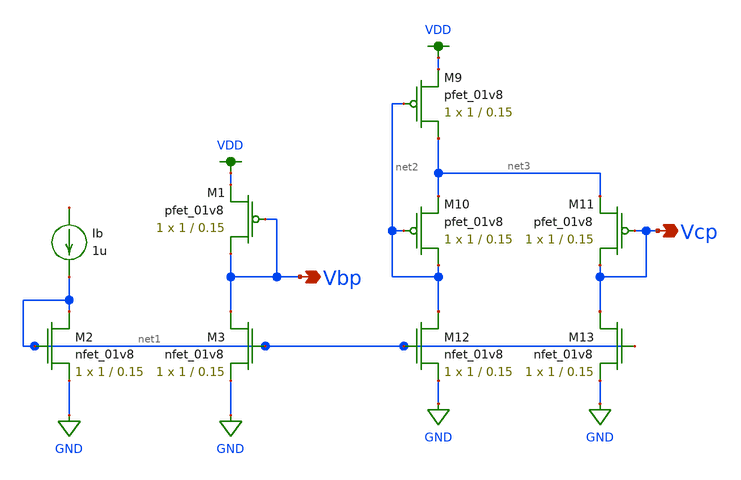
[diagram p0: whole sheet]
** sch_path: simulation/dac/cascode_v_gen.sch
**.subckt cascode_v_gen Vcp Vbp
*.opin Vcp
*.opin Vbp
XM1 Vbp Vbp VDD VDD sky130_fd_pr__pfet_01v8 L=0.15 W=1 nf=1 ad='int((nf+1)/2) * W/nf * 0.29' as='int((nf+2)/2) * W/nf * 0.29'
+ pd='2*int((nf+1)/2) * (W/nf + 0.29)' ps='2*int((nf+2)/2) * (W/nf + 0.29)' nrd='0.29 / W' nrs='0.29 / W'
+ sa=0 sb=0 sd=0 mult=1 m=1
XM2 net1 net1 GND GND sky130_fd_pr__nfet_01v8 L=0.15 W=1 nf=1 ad='int((nf+1)/2) * W/nf * 0.29' as='int((nf+2)/2) * W/nf * 0.29'
+ pd='2*int((nf+1)/2) * (W/nf + 0.29)' ps='2*int((nf+2)/2) * (W/nf + 0.29)' nrd='0.29 / W' nrs='0.29 / W'
+ sa=0 sb=0 sd=0 mult=1 m=1
XM3 Vbp net1 GND GND sky130_fd_pr__nfet_01v8 L=0.15 W=1 nf=1 ad='int((nf+1)/2) * W/nf * 0.29' as='int((nf+2)/2) * W/nf * 0.29'
+ pd='2*int((nf+1)/2) * (W/nf + 0.29)' ps='2*int((nf+2)/2) * (W/nf + 0.29)' nrd='0.29 / W' nrs='0.29 / W'
+ sa=0 sb=0 sd=0 mult=1 m=1
XM9 net3 net2 VDD VDD sky130_fd_pr__pfet_01v8 L=0.15 W=1 nf=1 ad='int((nf+1)/2) * W/nf * 0.29' as='int((nf+2)/2) * W/nf * 0.29'
+ pd='2*int((nf+1)/2) * (W/nf + 0.29)' ps='2*int((nf+2)/2) * (W/nf + 0.29)' nrd='0.29 / W' nrs='0.29 / W'
+ sa=0 sb=0 sd=0 mult=1 m=1
XM10 net2 net2 net3 VDD sky130_fd_pr__pfet_01v8 L=0.15 W=1 nf=1 ad='int((nf+1)/2) * W/nf * 0.29' as='int((nf+2)/2) * W/nf * 0.29'
+ pd='2*int((nf+1)/2) * (W/nf + 0.29)' ps='2*int((nf+2)/2) * (W/nf + 0.29)' nrd='0.29 / W' nrs='0.29 / W'
+ sa=0 sb=0 sd=0 mult=1 m=1
XM11 Vcp Vcp net3 VDD sky130_fd_pr__pfet_01v8 L=0.15 W=1 nf=1 ad='int((nf+1)/2) * W/nf * 0.29' as='int((nf+2)/2) * W/nf * 0.29'
+ pd='2*int((nf+1)/2) * (W/nf + 0.29)' ps='2*int((nf+2)/2) * (W/nf + 0.29)' nrd='0.29 / W' nrs='0.29 / W'
+ sa=0 sb=0 sd=0 mult=1 m=1
XM12 net2 net1 GND GND sky130_fd_pr__nfet_01v8 L=0.15 W=1 nf=1 ad='int((nf+1)/2) * W/nf * 0.29' as='int((nf+2)/2) * W/nf * 0.29'
+ pd='2*int((nf+1)/2) * (W/nf + 0.29)' ps='2*int((nf+2)/2) * (W/nf + 0.29)' nrd='0.29 / W' nrs='0.29 / W'
+ sa=0 sb=0 sd=0 mult=1 m=1
XM13 Vcp net1 GND GND sky130_fd_pr__nfet_01v8 L=0.15 W=1 nf=1 ad='int((nf+1)/2) * W/nf * 0.29' as='int((nf+2)/2) * W/nf * 0.29'
+ pd='2*int((nf+1)/2) * (W/nf + 0.29)' ps='2*int((nf+2)/2) * (W/nf + 0.29)' nrd='0.29 / W' nrs='0.29 / W'
+ sa=0 sb=0 sd=0 mult=1 m=1
Ib net4 net1 1u
**.ends
.GLOBAL VDD
.GLOBAL GND
.end
